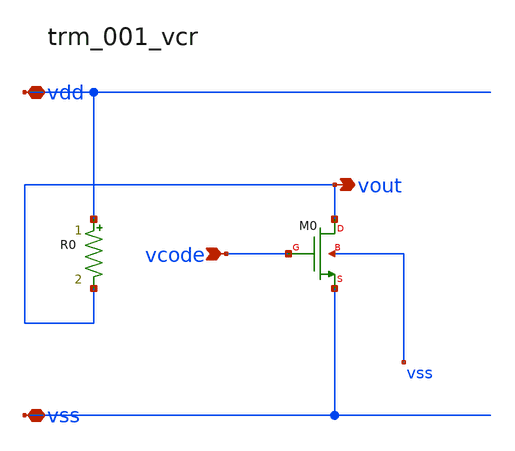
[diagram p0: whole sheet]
** sch_path: analog-db/raw/trm_001_vcr/trm_001_vcr_annotated.sch
**.subckt trm_001_vcr_annotated vcode vdd vss vout
*.ipin vcode
*.iopin vdd
*.iopin vss
*.opin vout
R0 vdd vout x_dut_r0_value m=1
XM0 vout vcode vss vss sg13_lv_nmos w=x_dut_xm0_w l=x_dut_xm0_l ng=1 m=x_dut_xm0_m
**.ends
.end
